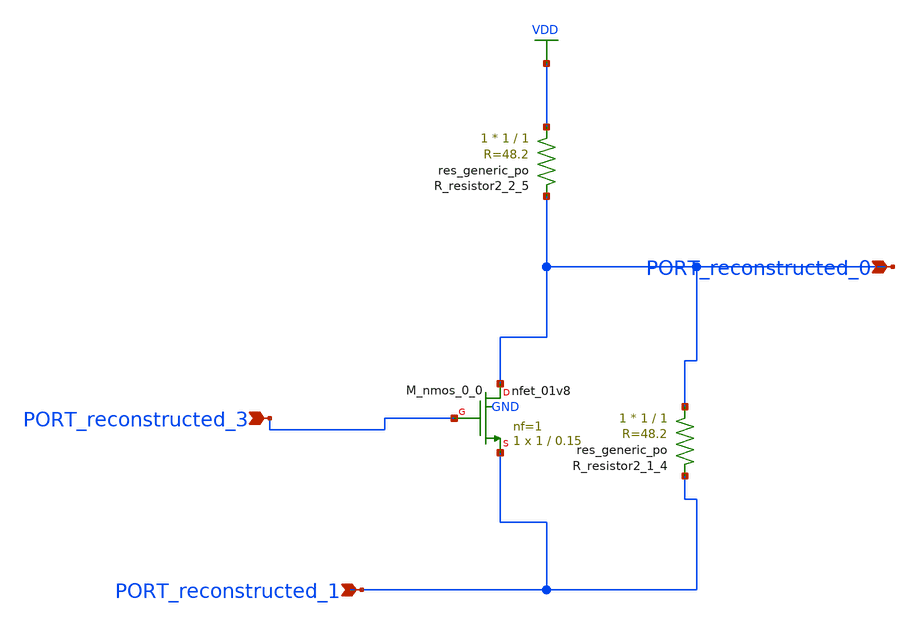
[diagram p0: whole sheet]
** sch_path: schematics/AMSNet/146.sch
**.subckt 146 PORT_reconstructed_3 PORT_reconstructed_1 PORT_reconstructed_0
*.ipin PORT_reconstructed_3
*.ipin PORT_reconstructed_1
*.ipin PORT_reconstructed_0
XM_nmos_0_0 PORT_reconstructed_0 PORT_reconstructed_3 PORT_reconstructed_1 GND sky130_fd_pr__nfet_01v8
+ L=0.15 W=1 nf=1 ad='int((1 + 1)/2) * 1 / 1 * 0.29' as='int((1 + 2)/2) * 1 / 1 * 0.29' pd='2*int((1 + 1)/2) * (1 / 1 + 0.29)'
+ ps='2*int((1 + 2)/2) * (1 / 1 + 0.29)' nrd='0.29 / 1 ' nrs='0.29 / 1 ' sa=0 sb=0 sd=0 mult=1 m=1
XR_resistor2_1_4 PORT_reconstructed_0 PORT_reconstructed_1 sky130_fd_pr__res_generic_po W=1 L=1 m=1
XR_resistor2_2_5 VDD PORT_reconstructed_0 sky130_fd_pr__res_generic_po W=1 L=1 m=1
**.ends
.GLOBAL VDD
.end
